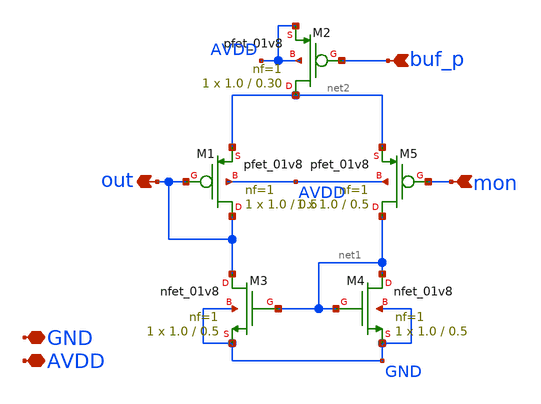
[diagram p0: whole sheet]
** sch_path: design/xschem/buffer_mon_p_norail.sch
**.subckt buffer_mon_p_norail GND AVDD buf_p mon out
*.iopin GND
*.iopin AVDD
*.ipin buf_p
*.ipin mon
*.opin out
XM1 out out net2 AVDD sky130_fd_pr__pfet_01v8 L=0.5 W=1.0 nf=1 ad='int((nf+1)/2) * W/nf * 0.29' as='int((nf+2)/2) * W/nf * 0.29'
+ pd='2*int((nf+1)/2) * (W/nf + 0.29)' ps='2*int((nf+2)/2) * (W/nf + 0.29)' nrd='0.29 / W' nrs='0.29 / W'
+ sa=0 sb=0 sd=0 mult=1 m=1
XM5 net1 mon net2 AVDD sky130_fd_pr__pfet_01v8 L=0.5 W=1.0 nf=1 ad='int((nf+1)/2) * W/nf * 0.29' as='int((nf+2)/2) * W/nf * 0.29'
+ pd='2*int((nf+1)/2) * (W/nf + 0.29)' ps='2*int((nf+2)/2) * (W/nf + 0.29)' nrd='0.29 / W' nrs='0.29 / W'
+ sa=0 sb=0 sd=0 mult=1 m=1
XM2 net2 buf_p AVDD AVDD sky130_fd_pr__pfet_01v8 L=0.30 W=1.0 nf=1 ad='int((nf+1)/2) * W/nf * 0.29' as='int((nf+2)/2) * W/nf * 0.29'
+ pd='2*int((nf+1)/2) * (W/nf + 0.29)' ps='2*int((nf+2)/2) * (W/nf + 0.29)' nrd='0.29 / W' nrs='0.29 / W'
+ sa=0 sb=0 sd=0 mult=1 m=1
XM3 out net1 GND GND sky130_fd_pr__nfet_01v8 L=0.5 W=1.0 nf=1 ad='int((nf+1)/2) * W/nf * 0.29' as='int((nf+2)/2) * W/nf * 0.29'
+ pd='2*int((nf+1)/2) * (W/nf + 0.29)' ps='2*int((nf+2)/2) * (W/nf + 0.29)' nrd='0.29 / W' nrs='0.29 / W'
+ sa=0 sb=0 sd=0 mult=1 m=1
XM4 net1 net1 GND GND sky130_fd_pr__nfet_01v8 L=0.5 W=1.0 nf=1 ad='int((nf+1)/2) * W/nf * 0.29' as='int((nf+2)/2) * W/nf * 0.29'
+ pd='2*int((nf+1)/2) * (W/nf + 0.29)' ps='2*int((nf+2)/2) * (W/nf + 0.29)' nrd='0.29 / W' nrs='0.29 / W'
+ sa=0 sb=0 sd=0 mult=1 m=1
**.ends
.end
